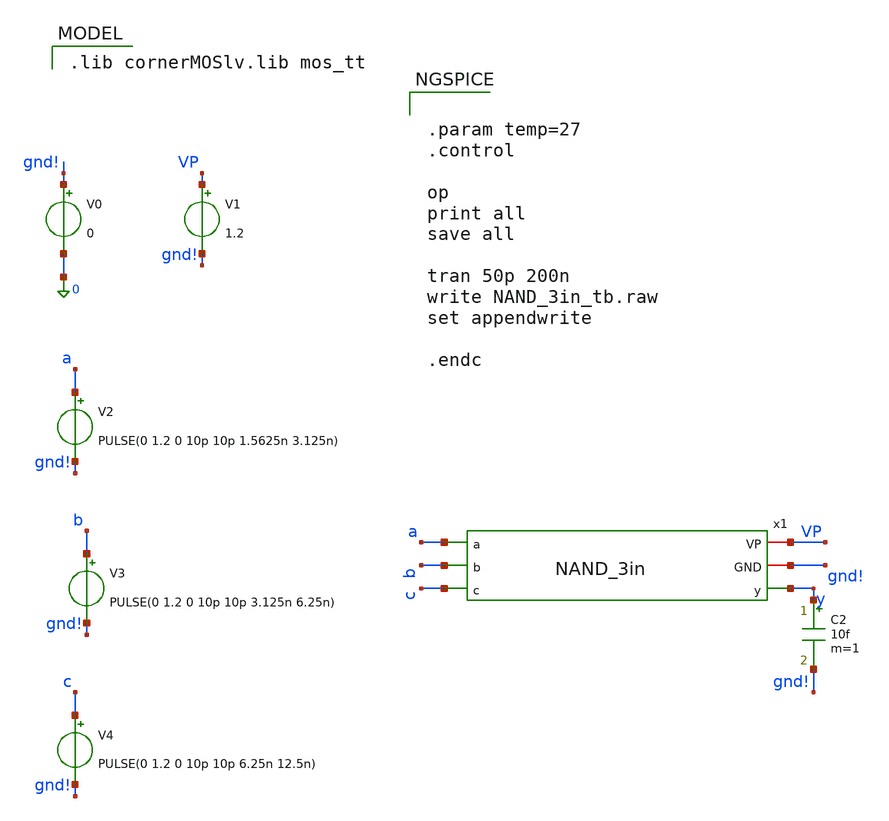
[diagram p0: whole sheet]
** sch_path: PLL0663-main/testbenches/tran/xschem/divider/NAND_3in_tb.sch
**.subckt NAND_3in_tb
V1 VP gnd! 1.2
V2 a gnd! PULSE(0 1.2 0 10p 10p 1.5625n 3.125n)
V0 gnd! 0 0
C2 y gnd! 10f m=1
V3 b gnd! PULSE(0 1.2 0 10p 10p 3.125n 6.25n)
V4 c gnd! PULSE(0 1.2 0 10p 10p 6.25n 12.5n)
x1 VP gnd! a y b c NAND_3in
**** begin user architecture code
 .lib cornerMOSlv.lib mos_tt



.param temp=27
.control

op
print all
save all

tran 50p 200n
write NAND_3in_tb.raw
set appendwrite

.endc


**** end user architecture code
**.ends
.end
